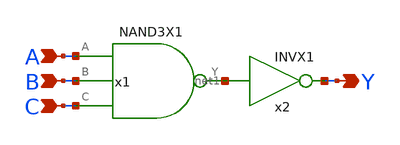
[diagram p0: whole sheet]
** sch_path: lib/xschem/AND3X1.sch
**.subckt AND3X1 A B C Y
*.ipin A
*.ipin B
*.ipin C
*.opin Y
x1 net1 A B C NAND3X1
x2 Y net1 INVX1
**.ends

* expanding   symbol:  NAND3X1.sym # of pins=4
** sym_path: lib/xschem/NAND3X1.sym
** sch_path: lib/xschem/NAND3X1.sch
.subckt NAND3X1 Y A B C
*.ipin A
*.opin Y
*.ipin B
*.ipin C
XM1 net2 C GND GND sky130_fd_pr__nfet_01v8 L=0.15 W=3 nf=1 ad='int((nf+1)/2) * W/nf * 0.29' as='int((nf+2)/2) * W/nf * 0.29'
+ pd='2*int((nf+1)/2) * (W/nf + 0.29)' ps='2*int((nf+2)/2) * (W/nf + 0.29)' nrd='0.29 / W' nrs='0.29 / W'
+ sa=0 sb=0 sd=0 mult=1 m=1
XM2 Y A VDD VDD sky130_fd_pr__pfet_01v8 L=0.15 W=2 nf=1 ad='int((nf+1)/2) * W/nf * 0.29' as='int((nf+2)/2) * W/nf * 0.29'
+ pd='2*int((nf+1)/2) * (W/nf + 0.29)' ps='2*int((nf+2)/2) * (W/nf + 0.29)' nrd='0.29 / W' nrs='0.29 / W'
+ sa=0 sb=0 sd=0 mult=1 m=1
XM3 net1 B net2 GND sky130_fd_pr__nfet_01v8 L=0.15 W=3 nf=1 ad='int((nf+1)/2) * W/nf * 0.29' as='int((nf+2)/2) * W/nf * 0.29'
+ pd='2*int((nf+1)/2) * (W/nf + 0.29)' ps='2*int((nf+2)/2) * (W/nf + 0.29)' nrd='0.29 / W' nrs='0.29 / W'
+ sa=0 sb=0 sd=0 mult=1 m=1
XM4 Y A net1 GND sky130_fd_pr__nfet_01v8 L=0.15 W=3 nf=1 ad='int((nf+1)/2) * W/nf * 0.29' as='int((nf+2)/2) * W/nf * 0.29'
+ pd='2*int((nf+1)/2) * (W/nf + 0.29)' ps='2*int((nf+2)/2) * (W/nf + 0.29)' nrd='0.29 / W' nrs='0.29 / W'
+ sa=0 sb=0 sd=0 mult=1 m=1
XM5 Y A VDD VDD sky130_fd_pr__pfet_01v8 L=0.15 W=2 nf=1 ad='int((nf+1)/2) * W/nf * 0.29' as='int((nf+2)/2) * W/nf * 0.29'
+ pd='2*int((nf+1)/2) * (W/nf + 0.29)' ps='2*int((nf+2)/2) * (W/nf + 0.29)' nrd='0.29 / W' nrs='0.29 / W'
+ sa=0 sb=0 sd=0 mult=1 m=1
XM6 Y B VDD VDD sky130_fd_pr__pfet_01v8 L=0.15 W=2 nf=1 ad='int((nf+1)/2) * W/nf * 0.29' as='int((nf+2)/2) * W/nf * 0.29'
+ pd='2*int((nf+1)/2) * (W/nf + 0.29)' ps='2*int((nf+2)/2) * (W/nf + 0.29)' nrd='0.29 / W' nrs='0.29 / W'
+ sa=0 sb=0 sd=0 mult=1 m=1
XM7 Y B VDD VDD sky130_fd_pr__pfet_01v8 L=0.15 W=2 nf=1 ad='int((nf+1)/2) * W/nf * 0.29' as='int((nf+2)/2) * W/nf * 0.29'
+ pd='2*int((nf+1)/2) * (W/nf + 0.29)' ps='2*int((nf+2)/2) * (W/nf + 0.29)' nrd='0.29 / W' nrs='0.29 / W'
+ sa=0 sb=0 sd=0 mult=1 m=1
XM8 Y C VDD VDD sky130_fd_pr__pfet_01v8 L=0.15 W=2 nf=1 ad='int((nf+1)/2) * W/nf * 0.29' as='int((nf+2)/2) * W/nf * 0.29'
+ pd='2*int((nf+1)/2) * (W/nf + 0.29)' ps='2*int((nf+2)/2) * (W/nf + 0.29)' nrd='0.29 / W' nrs='0.29 / W'
+ sa=0 sb=0 sd=0 mult=1 m=1
XM9 Y C VDD VDD sky130_fd_pr__pfet_01v8 L=0.15 W=2 nf=1 ad='int((nf+1)/2) * W/nf * 0.29' as='int((nf+2)/2) * W/nf * 0.29'
+ pd='2*int((nf+1)/2) * (W/nf + 0.29)' ps='2*int((nf+2)/2) * (W/nf + 0.29)' nrd='0.29 / W' nrs='0.29 / W'
+ sa=0 sb=0 sd=0 mult=1 m=1
.ends

.GLOBAL VDD
.GLOBAL GND
.end
